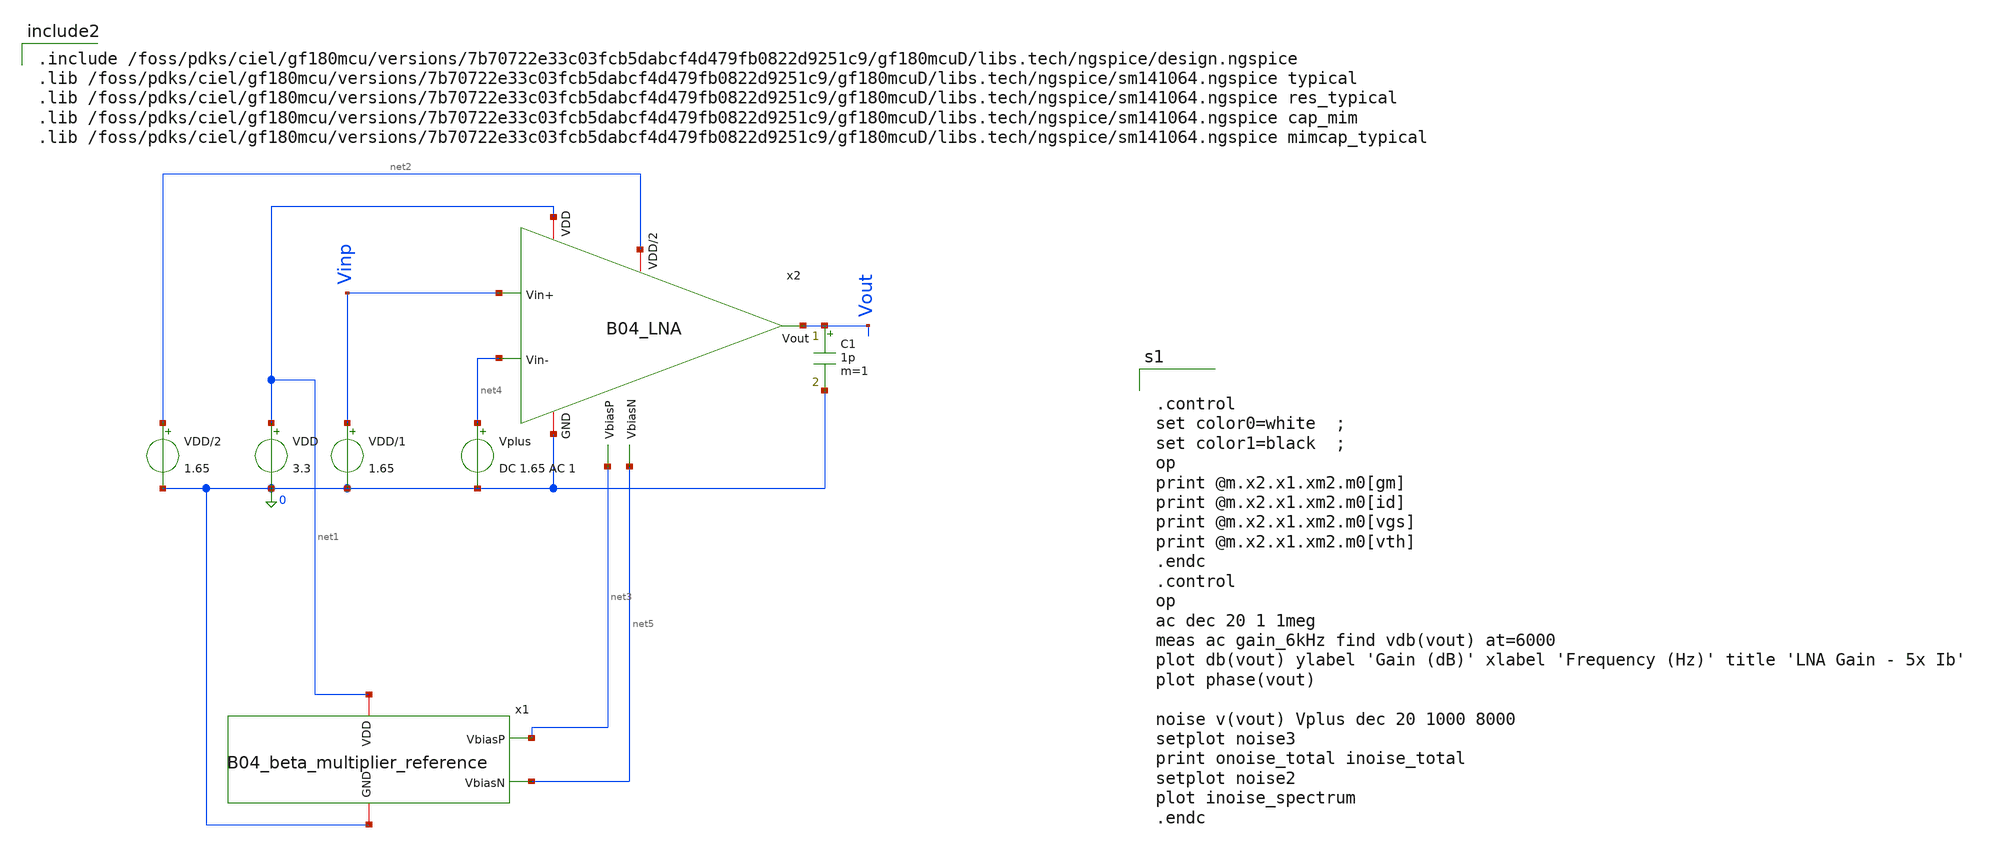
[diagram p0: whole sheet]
** sch_path: analog/B04_tb_LNA.sch
**.subckt B04_tb_LNA
VDD net1 0 3.3
Vplus net4 0 DC 1.65 AC 1
x2 net1 net2 Vinp Vout net4 0 net3 net5 B04_LNA
VDD/2 net2 0 1.65
VDD/1 Vinp 0 1.65
x1 net1 net3 net5 0 B04_beta_multiplier_reference length=410u
C1 Vout 0 1p m=1
**** begin user architecture code


.control
set color0=white  ;
set color1=black  ;
op
print @m.x2.x1.xm2.m0[gm]
print @m.x2.x1.xm2.m0[id]
print @m.x2.x1.xm2.m0[vgs]
print @m.x2.x1.xm2.m0[vth]
.endc
.control
op
ac dec 20 1 1meg
meas ac gain_6kHz find vdb(vout) at=6000
plot db(vout) ylabel 'Gain (dB)' xlabel 'Frequency (Hz)' title 'LNA Gain - 5x Ib'
plot phase(vout)

noise v(vout) Vplus dec 20 1000 8000
setplot noise3
print onoise_total inoise_total
setplot noise2
plot inoise_spectrum
.endc



.include /foss/pdks/ciel/gf180mcu/versions/7b70722e33c03fcb5dabcf4d479fb0822d9251c9/gf180mcuD/libs.tech/ngspice/design.ngspice
.lib /foss/pdks/ciel/gf180mcu/versions/7b70722e33c03fcb5dabcf4d479fb0822d9251c9/gf180mcuD/libs.tech/ngspice/sm141064.ngspice typical
.lib /foss/pdks/ciel/gf180mcu/versions/7b70722e33c03fcb5dabcf4d479fb0822d9251c9/gf180mcuD/libs.tech/ngspice/sm141064.ngspice res_typical
.lib /foss/pdks/ciel/gf180mcu/versions/7b70722e33c03fcb5dabcf4d479fb0822d9251c9/gf180mcuD/libs.tech/ngspice/sm141064.ngspice cap_mim
.lib /foss/pdks/ciel/gf180mcu/versions/7b70722e33c03fcb5dabcf4d479fb0822d9251c9/gf180mcuD/libs.tech/ngspice/sm141064.ngspice mimcap_typical

**** end user architecture code
**.ends
.end
